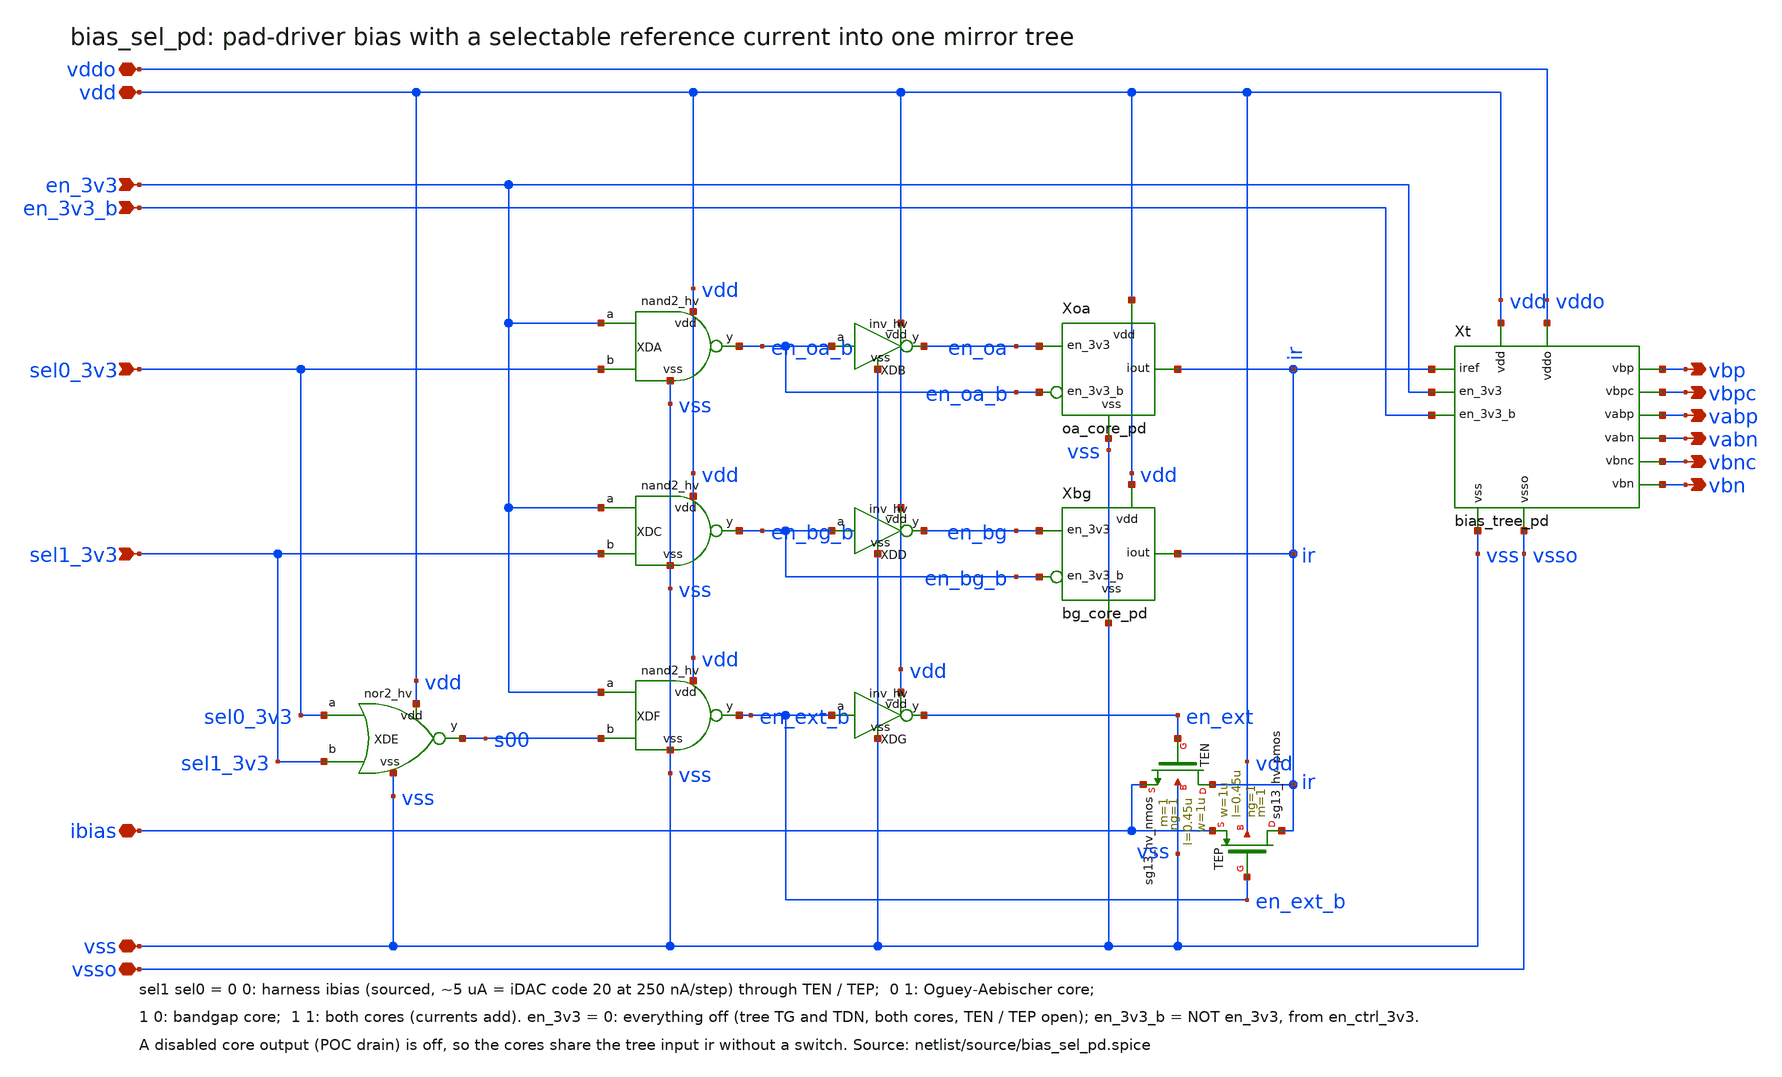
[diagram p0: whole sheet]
** sch_path: sudelbuecher/design_considerations/consolidation/ab_regroup_2026-10-28/before/macros/bias_sel_pd/schematic/xschem/bias_sel_pd.sch
**.subckt bias_sel_pd vdd vss vddo vsso ibias vbp vbn vbpc vbnc vabp vabn en_3v3 sel0_3v3 sel1_3v3
*+ en_3v3_b
*.iopin vdd
*.iopin vss
*.iopin vddo
*.iopin vsso
*.iopin ibias
*.opin vbp
*.opin vbn
*.opin vbpc
*.opin vbnc
*.opin vabp
*.opin vabn
*.ipin en_3v3
*.ipin sel0_3v3
*.ipin sel1_3v3
*.ipin en_3v3_b
Xt vdd vss vddo vsso ir vbp vbn vbpc vbnc vabp vabn en_3v3 en_3v3_b bias_tree_pd
XDA vdd vss en_3v3 sel0_3v3 en_oa_b nand2_hv
XDB vdd vss en_oa_b en_oa inv_hv
XDC vdd vss en_3v3 sel1_3v3 en_bg_b nand2_hv
XDD vdd vss en_bg_b en_bg inv_hv
XDE vdd vss sel0_3v3 sel1_3v3 s00 nor2_hv
XDF vdd vss en_3v3 s00 en_ext_b nand2_hv
XDG vdd vss en_ext_b en_ext inv_hv
Xoa vdd vss ir en_oa en_oa_b oa_core_pd
Xbg vdd vss ir en_bg en_bg_b bg_core_pd
XTEN ir en_ext ibias vss sg13_hv_nmos w=1u l=0.45u ng=1 m=1 mm_ok=1
XTEP ir en_ext_b ibias vdd sg13_hv_pmos w=1u l=0.45u ng=1 m=1 mm_ok=1
**.ends
.end
